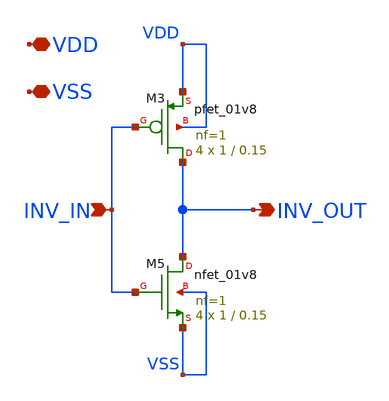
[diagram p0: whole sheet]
** sch_path: xschem/inv_x4.sch
**.subckt inv_x4 INV_IN INV_OUT VDD VSS
*.ipin INV_IN
*.opin INV_OUT
*.iopin VDD
*.iopin VSS
XM3 INV_OUT INV_IN VDD VDD sky130_fd_pr__pfet_01v8 L=0.15 W=1 nf=1 ad='int((nf+1)/2) * W/nf * 0.29' as='int((nf+2)/2) * W/nf * 0.29'
+ pd='2*int((nf+1)/2) * (W/nf + 0.29)' ps='2*int((nf+2)/2) * (W/nf + 0.29)' nrd='0.29 / W' nrs='0.29 / W'
+ sa=0 sb=0 sd=0 mult=4 m=4
XM5 INV_OUT INV_IN VSS VSS sky130_fd_pr__nfet_01v8 L=0.15 W=1 nf=1 ad='int((nf+1)/2) * W/nf * 0.29' as='int((nf+2)/2) * W/nf * 0.29'
+ pd='2*int((nf+1)/2) * (W/nf + 0.29)' ps='2*int((nf+2)/2) * (W/nf + 0.29)' nrd='0.29 / W' nrs='0.29 / W'
+ sa=0 sb=0 sd=0 mult=4 m=4
**.ends
.end
